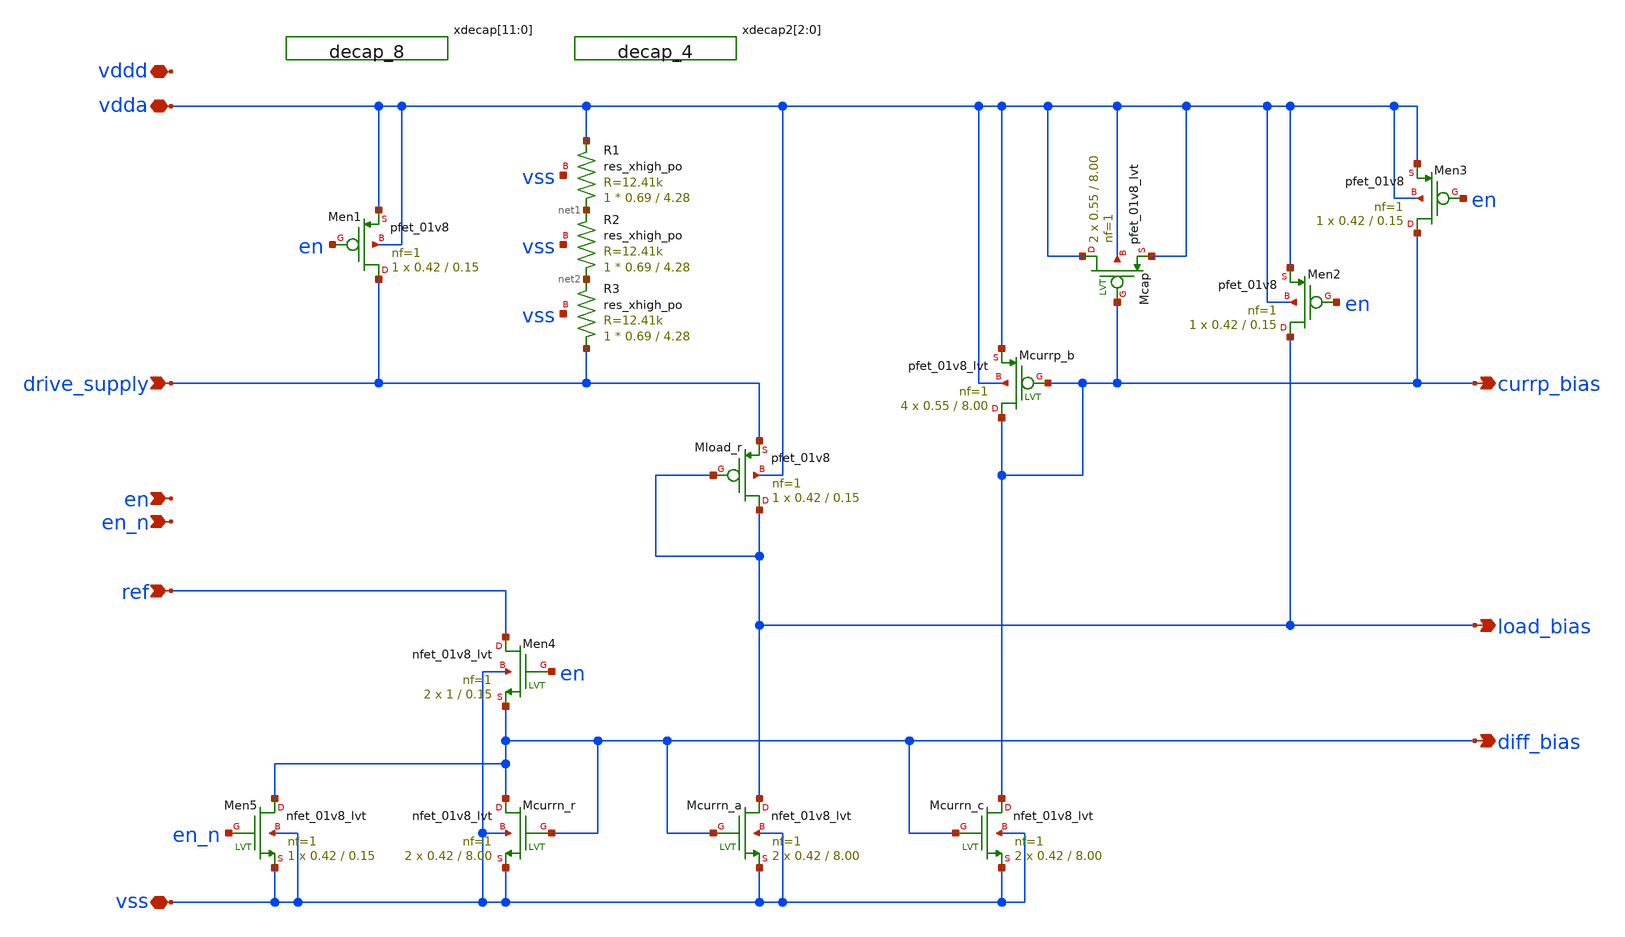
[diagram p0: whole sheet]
** sch_path: design/dac_bias/dac_bias.sch
**.subckt dac_bias vdda vss currp_bias ref load_bias drive_supply vddd en en_n diff_bias
*.iopin vdda
*.iopin vss
*.opin currp_bias
*.ipin ref
*.opin load_bias
*.ipin drive_supply
*.iopin vddd
*.ipin en
*.ipin en_n
*.opin diff_bias
XMcurrp_b currp_bias currp_bias vdda vdda sky130_fd_pr__pfet_01v8_lvt L=8.00 W=0.55 nf=1 ad='int((nf+1)/2) * W/nf * 0.29'
+ as='int((nf+2)/2) * W/nf * 0.29' pd='2*int((nf+1)/2) * (W/nf + 0.29)' ps='2*int((nf+2)/2) * (W/nf + 0.29)'
+ nrd='0.29 / W' nrs='0.29 / W' sa=0 sb=0 sd=0 mult=4 m=4
XMcurrn_r diff_bias diff_bias vss vss sky130_fd_pr__nfet_01v8_lvt L=8.00 W=0.42 nf=1 ad='int((nf+1)/2) * W/nf * 0.29'
+ as='int((nf+2)/2) * W/nf * 0.29' pd='2*int((nf+1)/2) * (W/nf + 0.29)' ps='2*int((nf+2)/2) * (W/nf + 0.29)'
+ nrd='0.29 / W' nrs='0.29 / W' sa=0 sb=0 sd=0 mult=2 m=2
XMcurrn_c currp_bias diff_bias vss vss sky130_fd_pr__nfet_01v8_lvt L=8.00 W=0.42 nf=1 ad='int((nf+1)/2) * W/nf * 0.29'
+ as='int((nf+2)/2) * W/nf * 0.29' pd='2*int((nf+1)/2) * (W/nf + 0.29)' ps='2*int((nf+2)/2) * (W/nf + 0.29)'
+ nrd='0.29 / W' nrs='0.29 / W' sa=0 sb=0 sd=0 mult=2 m=2
XMcurrn_a load_bias diff_bias vss vss sky130_fd_pr__nfet_01v8_lvt L=8.00 W=0.42 nf=1 ad='int((nf+1)/2) * W/nf * 0.29'
+ as='int((nf+2)/2) * W/nf * 0.29' pd='2*int((nf+1)/2) * (W/nf + 0.29)' ps='2*int((nf+2)/2) * (W/nf + 0.29)'
+ nrd='0.29 / W' nrs='0.29 / W' sa=0 sb=0 sd=0 mult=2 m=2
XMload_r load_bias load_bias drive_supply vdda sky130_fd_pr__pfet_01v8 L=0.15 W=0.42 nf=1 ad='W * 0.29'
+ as='W * 0.29' pd='2 * (W + 0.29)' ps='2 * (W + 0.29)' nrd='0.29 / W' nrs='0.29 / W' sa=0 sb=0 sd=0 mult=1
+ m=1
XMcap vdda currp_bias vdda vdda sky130_fd_pr__pfet_01v8_lvt L=8.00 W=0.55 nf=1 ad='int((nf+1)/2) * W/nf * 0.29'
+ as='int((nf+2)/2) * W/nf * 0.29' pd='2*int((nf+1)/2) * (W/nf + 0.29)' ps='2*int((nf+2)/2) * (W/nf + 0.29)'
+ nrd='0.29 / W' nrs='0.29 / W' sa=0 sb=0 sd=0 mult=2 m=2
xdecap[11] vss vss vddd vddd sky130_fd_sc_hs__decap_8
xdecap[10] vss vss vddd vddd sky130_fd_sc_hs__decap_8
xdecap[9] vss vss vddd vddd sky130_fd_sc_hs__decap_8
xdecap[8] vss vss vddd vddd sky130_fd_sc_hs__decap_8
xdecap[7] vss vss vddd vddd sky130_fd_sc_hs__decap_8
xdecap[6] vss vss vddd vddd sky130_fd_sc_hs__decap_8
xdecap[5] vss vss vddd vddd sky130_fd_sc_hs__decap_8
xdecap[4] vss vss vddd vddd sky130_fd_sc_hs__decap_8
xdecap[3] vss vss vddd vddd sky130_fd_sc_hs__decap_8
xdecap[2] vss vss vddd vddd sky130_fd_sc_hs__decap_8
xdecap[1] vss vss vddd vddd sky130_fd_sc_hs__decap_8
xdecap[0] vss vss vddd vddd sky130_fd_sc_hs__decap_8
xdecap2[2] vss vss vddd vddd sky130_fd_sc_hs__decap_4
xdecap2[1] vss vss vddd vddd sky130_fd_sc_hs__decap_4
xdecap2[0] vss vss vddd vddd sky130_fd_sc_hs__decap_4
XR1 net1 vdda vss sky130_fd_pr__res_xhigh_po W=0.69 L=4.28 mult=1 m=1
XR2 net2 net1 vss sky130_fd_pr__res_xhigh_po W=0.69 L=4.28 mult=1 m=1
XR3 drive_supply net2 vss sky130_fd_pr__res_xhigh_po W=0.69 L=4.28 mult=1 m=1
XMen4 ref en diff_bias vss sky130_fd_pr__nfet_01v8_lvt L=0.15 W=1 nf=1 ad='int((nf+1)/2) * W/nf * 0.29'
+ as='int((nf+2)/2) * W/nf * 0.29' pd='2*int((nf+1)/2) * (W/nf + 0.29)' ps='2*int((nf+2)/2) * (W/nf + 0.29)'
+ nrd='0.29 / W' nrs='0.29 / W' sa=0 sb=0 sd=0 mult=2 m=2
XMen1 drive_supply en vdda vdda sky130_fd_pr__pfet_01v8 L=0.15 W=0.42 nf=1 ad='W * 0.29' as='W * 0.29'
+ pd='2 * (W + 0.29)' ps='2 * (W + 0.29)' nrd='0.29 / W' nrs='0.29 / W' sa=0 sb=0 sd=0 mult=1 m=1
XMen5 diff_bias en_n vss vss sky130_fd_pr__nfet_01v8_lvt L=0.15 W=0.42 nf=1 ad='int((nf+1)/2) * W/nf * 0.29'
+ as='int((nf+2)/2) * W/nf * 0.29' pd='2*int((nf+1)/2) * (W/nf + 0.29)' ps='2*int((nf+2)/2) * (W/nf + 0.29)'
+ nrd='0.29 / W' nrs='0.29 / W' sa=0 sb=0 sd=0 mult=1 m=1
XMen2 load_bias en vdda vdda sky130_fd_pr__pfet_01v8 L=0.15 W=0.42 nf=1 ad='W * 0.29' as='W * 0.29' pd='2 * (W + 0.29)'
+ ps='2 * (W + 0.29)' nrd='0.29 / W' nrs='0.29 / W' sa=0 sb=0 sd=0 mult=1 m=1
XMen3 currp_bias en vdda vdda sky130_fd_pr__pfet_01v8 L=0.15 W=0.42 nf=1 ad='W * 0.29' as='W * 0.29'
+ pd='2 * (W + 0.29)' ps='2 * (W + 0.29)' nrd='0.29 / W' nrs='0.29 / W' sa=0 sb=0 sd=0 mult=1 m=1
**.ends
.end
